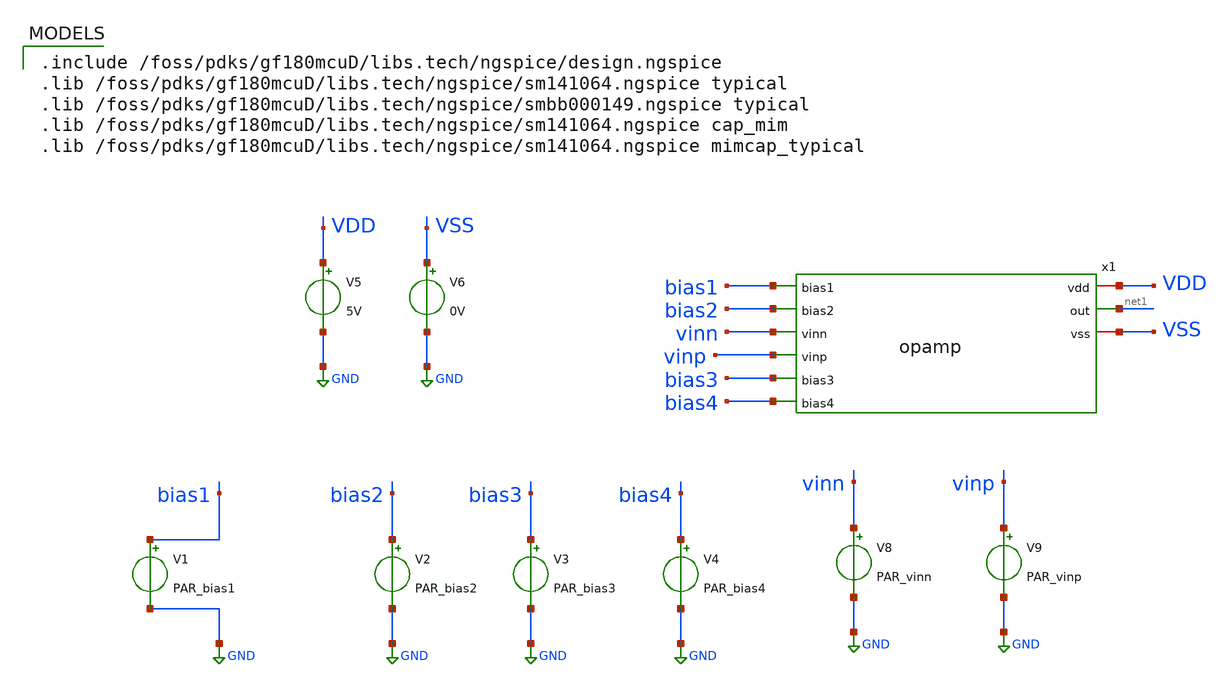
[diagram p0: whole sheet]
** sch_path: activities/opamp2AKAM/simulations_testbench/simulations_testbench/testingBias4.sch
**.subckt testingBias4
V1 bias1 GND PAR_bias1
V2 bias2 GND PAR_bias2
V3 bias3 GND PAR_bias3
V4 bias4 GND PAR_bias4
V5 VDD GND 5V
V6 VSS GND 0V
V8 vinn GND PAR_vinn
V9 vinp GND PAR_vinp
x1 VDD bias1 bias2 vinn net1 vinp bias3 bias4 VSS opamp
**** begin user architecture code

.include /foss/pdks/gf180mcuD/libs.tech/ngspice/design.ngspice
.lib /foss/pdks/gf180mcuD/libs.tech/ngspice/sm141064.ngspice typical
.lib /foss/pdks/gf180mcuD/libs.tech/ngspice/smbb000149.ngspice typical
.lib /foss/pdks/gf180mcuD/libs.tech/ngspice/sm141064.ngspice cap_mim
.lib /foss/pdks/gf180mcuD/libs.tech/ngspice/sm141064.ngspice mimcap_typical


** PARAMETERS
.PARAM PAR_bias1=3.425
.PARAM PAR_bias2=3.425
.PARAM PAR_bias3=3.425
.PARAM PAR_bias4=3.425
.PARAM PAR_vinn=2.5
.PARAM PAR_vinp=2.5

.control
 let x=0
 alter V1 = 3.425
 alter V2 = 2.428
 alter V3 = 1.909
 echo "bias4Value Gain" >
+ /foss/designs/sscs-2026-zotnetic/activities/opamp2AKAM/simulations_testbench/simulation_results/tuningBias4.txt
 while x<3.001
  alter V4=x
  dc V9 0 5 0.001
  meas dc vlo when v(net1)=1.5 cross=1
  meas dc vhi when v(net1)=3.5 cross=1
  let g = 2.0/abs(vhi-vlo)
  echo "$&x $&g"
+ >>/foss/designs/sscs-2026-zotnetic/activities/opamp2AKAM/simulations_testbench/simulation_results/tuningBias4.txt
  let x = x+0.05
  end
.endc

**** end user architecture code
**.ends
.GLOBAL GND
.end
